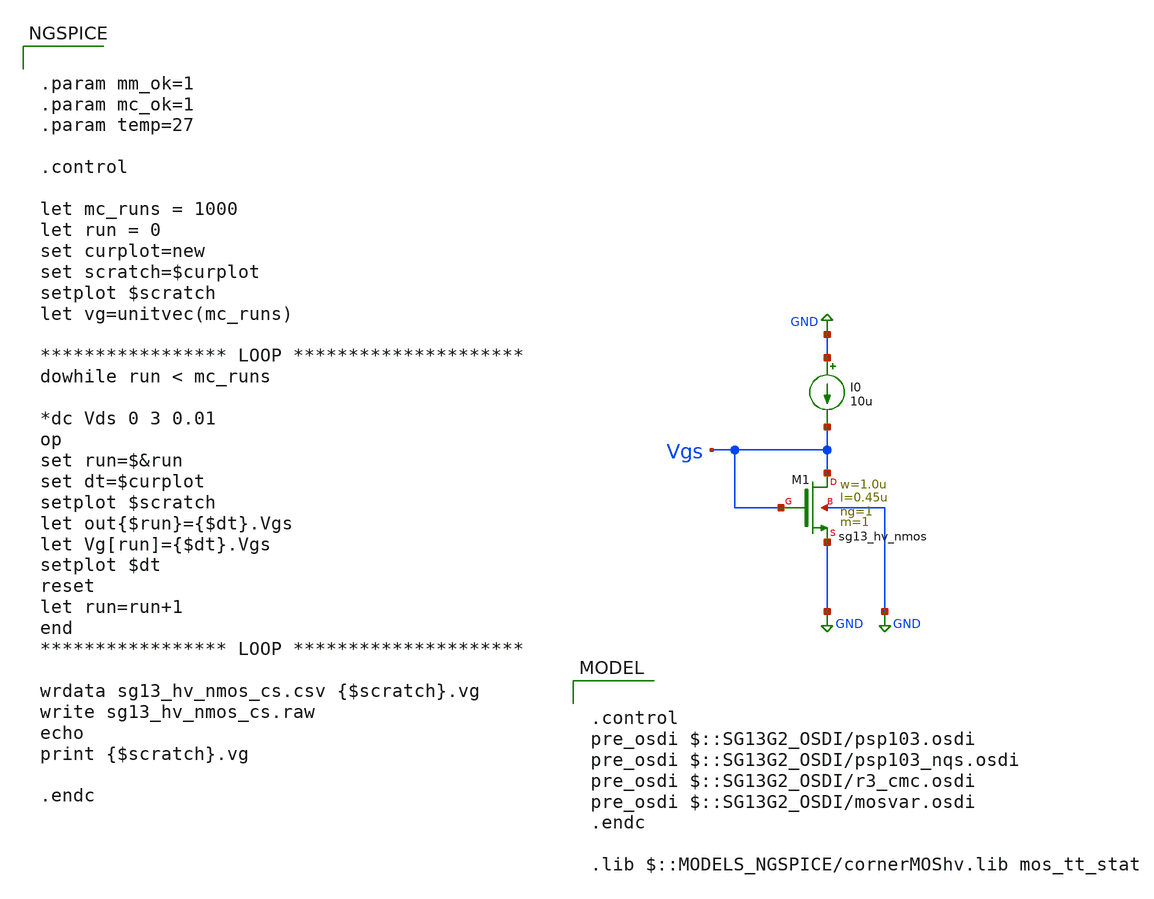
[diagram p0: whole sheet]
** sch_path: ihp-sg13g2/xschem_libs/sg13g2_tests/mc_hv_nmos_cs_loop/schematic/mc_hv_nmos_cs_loop.sch
* Copyright 2023 IHP PDK Authors
**.subckt mc_hv_nmos_cs_loop
I0 GND Vgs 10u
XM1 Vgs Vgs GND GND sg13_hv_nmos w=1.0u l=0.45u ng=1 m=1 mm_ok=1
**** begin user architecture code

.control
pre_osdi $::SG13G2_OSDI/psp103.osdi
pre_osdi $::SG13G2_OSDI/psp103_nqs.osdi
pre_osdi $::SG13G2_OSDI/r3_cmc.osdi
pre_osdi $::SG13G2_OSDI/mosvar.osdi
.endc

.lib $::MODELS_NGSPICE/cornerMOShv.lib mos_tt_stat




.param mm_ok=1
.param mc_ok=1
.param temp=27

.control

let mc_runs = 1000
let run = 0
set curplot=new
set scratch=$curplot
setplot $scratch
let vg=unitvec(mc_runs)

***************** LOOP *********************
dowhile run < mc_runs

*dc Vds 0 3 0.01
op
set run=$&run
set dt=$curplot
setplot $scratch
let out{$run}={$dt}.Vgs
let Vg[run]={$dt}.Vgs
setplot $dt
reset
let run=run+1
end
***************** LOOP *********************

wrdata sg13_hv_nmos_cs.csv {$scratch}.vg
write sg13_hv_nmos_cs.raw
echo
print {$scratch}.vg

.endc


**** end user architecture code
**.ends
.GLOBAL GND
.end
